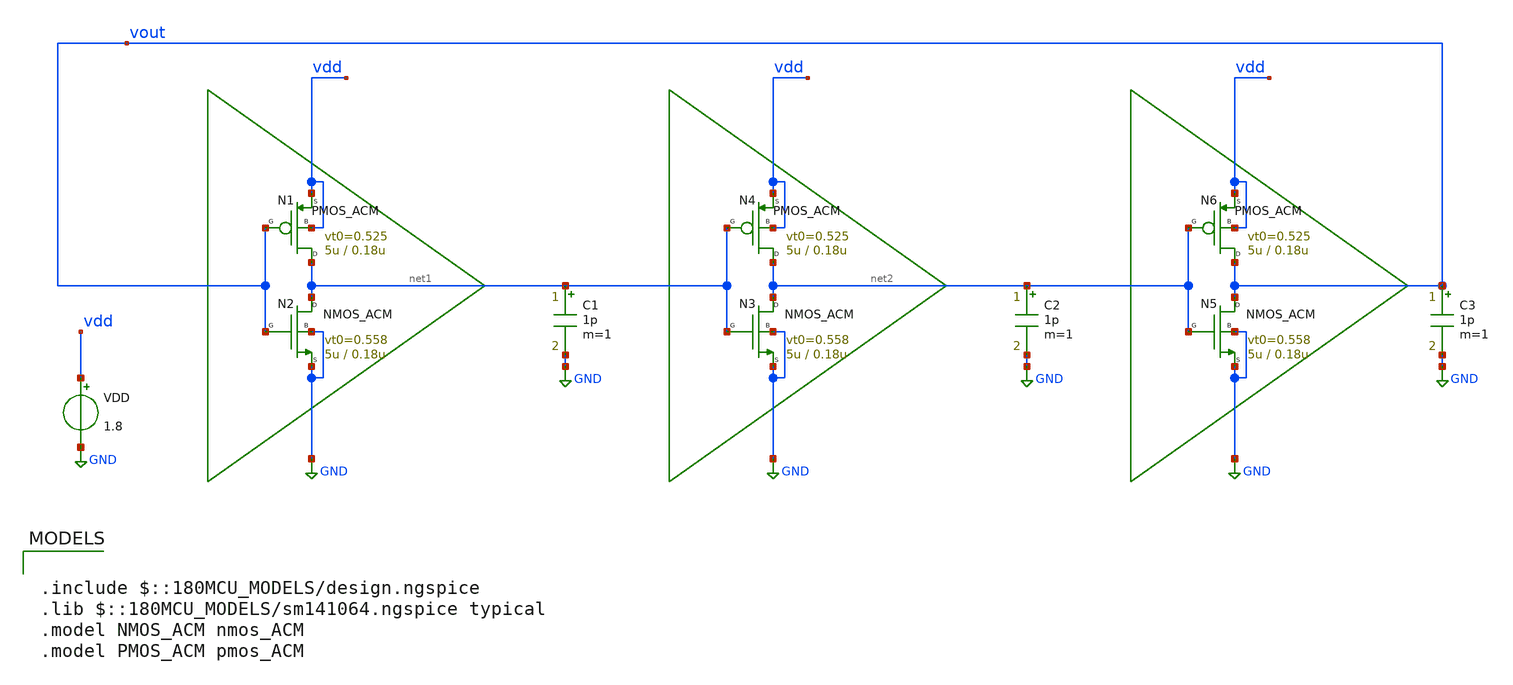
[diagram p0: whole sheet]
** sch_path: Examples/GF180MCU/xschem/TB_rosc_acm.sch
**.subckt TB_rosc_acm
VDD vdd GND 1.8
N2 net1 vout GND GND NMOS_ACM w=5u l=0.18u n=1.37 is=5.52u vt0=0.558 sigma=27m zeta={zeta_var}
N1 net1 vout vdd vdd PMOS_ACM w=5u l=0.18u n=1.40 is=1.82u vt0=0.525 sigma=24m zeta={zeta_var}
C1 net1 GND 1p m=1
N3 net2 net1 GND GND NMOS_ACM w=5u l=0.18u n=1.37 is=5.52u vt0=0.558 sigma=27m zeta={zeta_var}
N4 net2 net1 vdd vdd PMOS_ACM w=5u l=0.18u n=1.40 is=1.82u vt0=0.525 sigma=24m zeta={zeta_var}
C2 net2 GND 1p m=1
N5 vout net2 GND GND NMOS_ACM w=5u l=0.18u n=1.37 is=5.52u vt0=0.558 sigma=27m zeta={zeta_var}
N6 vout net2 vdd vdd PMOS_ACM w=5u l=0.18u n=1.40 is=1.82u vt0=0.525 sigma=24m zeta={zeta_var}
C3 vout GND 1p m=1
**** begin user architecture code

.include $::180MCU_MODELS/design.ngspice
.lib $::180MCU_MODELS/sm141064.ngspice typical
.model NMOS_ACM nmos_ACM
.model PMOS_ACM pmos_ACM




.param zeta_var = 0.1m

.ic V(vout)=1.65
.control
pre_osdi /home/gmaranhao/Documents/MOSFET_model/Examples/GF180MCU/xschem/symbol/NMOS_ACM_2V0.osdi
pre_osdi /home/gmaranhao/Documents/MOSFET_model/Examples/GF180MCU/xschem/symbol/PMOS_ACM_2V0.osdi
save all

tran 0.1p 20n
remzerovec
write TB_rosc_acm.raw

.endc


**** end user architecture code
**.ends
.GLOBAL GND
.end
